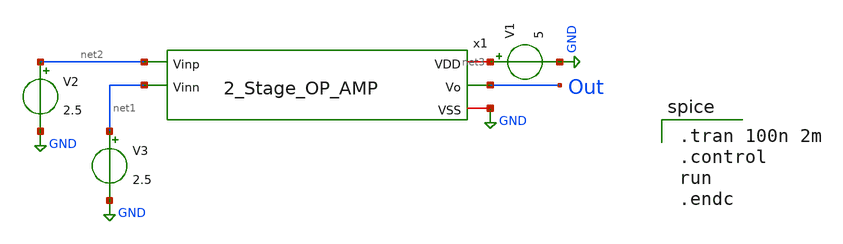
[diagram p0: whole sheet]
** sch_path: ADC/4bit_C2C/MagicAndSpice/EE431_FinalProj/OP_AMP_tb.sch
**.subckt OP_AMP_tb
V1 net3 GND 5
V2 net2 GND 2.5
V3 net1 GND 2.5
x1 net3 net2 net1 Out GND 2_Stage_OP_AMP
**** begin user architecture code
 .lib $::SKYWATER_MODELS/sky130.lib.spice tt

.tran 100n 2m
.control
run
.endc

**** end user architecture code
**.ends
.GLOBAL GND
.end
